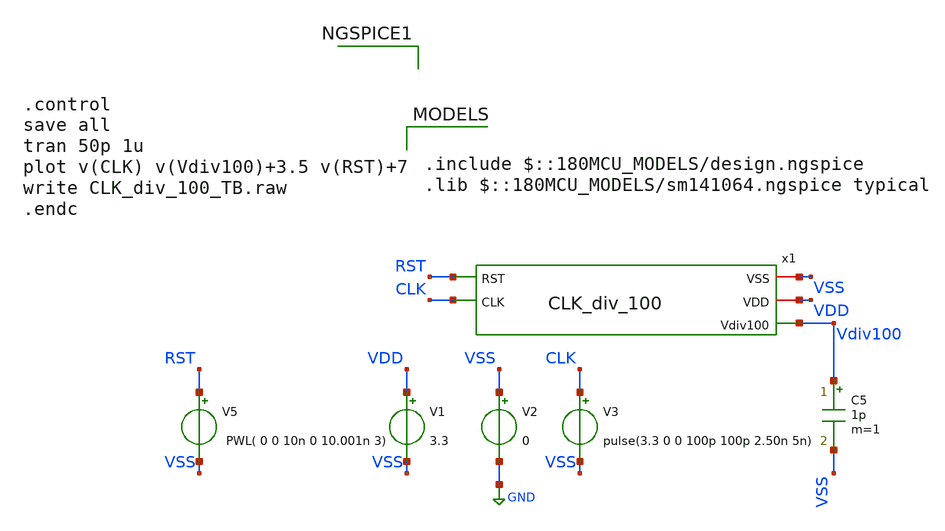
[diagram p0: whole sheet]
** sch_path: Clock_Generator_PAKISTAN_02/Schematics/CLK_div_100_TB.sch
**.subckt CLK_div_100_TB
V1 VDD VSS 3.3
V2 VSS GND 0
V3 CLK VSS pulse(3.3 0 0 100p 100p 2.50n 5n)
C5 Vdiv100 VSS 1p m=1
V5 RST VSS PWL( 0 0 10n 0 10.001n 3)
x1 VSS VDD RST Vdiv100 CLK CLK_div_100
**** begin user architecture code

.include $::180MCU_MODELS/design.ngspice
.lib $::180MCU_MODELS/sm141064.ngspice typical




.control
save all
tran 50p 1u
plot v(CLK) v(Vdiv100)+3.5 v(RST)+7
write CLK_div_100_TB.raw
.endc


**** end user architecture code
**.ends
.GLOBAL GND
.end
